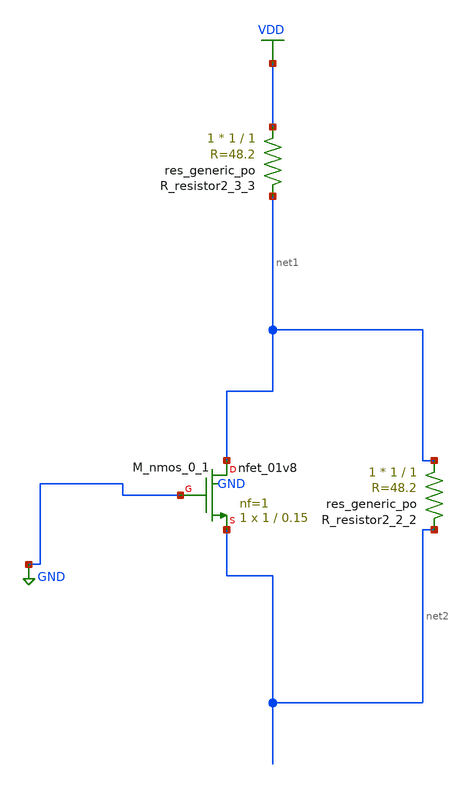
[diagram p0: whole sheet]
** sch_path: schematics/AMSNet/123.sch
**.subckt 123
XM_nmos_0_1 net1 GND net2 GND sky130_fd_pr__nfet_01v8 L=0.15 W=1 nf=1 ad='int((1 + 1)/2) * 1 / 1 * 0.29'
+ as='int((1 + 2)/2) * 1 / 1 * 0.29' pd='2*int((1 + 1)/2) * (1 / 1 + 0.29)' ps='2*int((1 + 2)/2) * (1 / 1 + 0.29)'
+ nrd='0.29 / 1 ' nrs='0.29 / 1 ' sa=0 sb=0 sd=0 mult=1 m=1
XR_resistor2_2_2 net1 net2 sky130_fd_pr__res_generic_po W=1 L=1 m=1
XR_resistor2_3_3 VDD net1 sky130_fd_pr__res_generic_po W=1 L=1 m=1
**.ends
.GLOBAL GND
.GLOBAL VDD
.end
